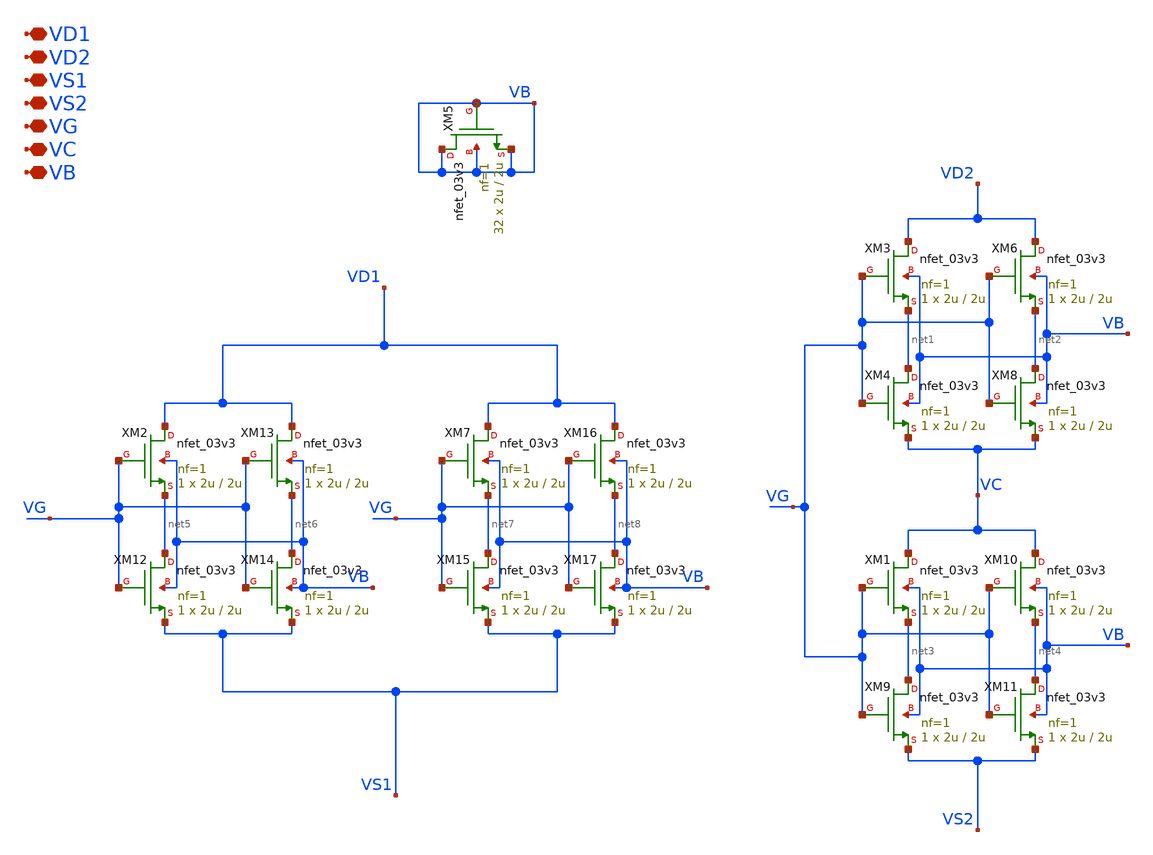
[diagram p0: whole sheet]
** sch_path: TIA_Filter/PseudoResistor/PR_nfets.sch
**.subckt PR_nfets VD1 VD2 VS1 VS2 VG VC VB
*.iopin VD1
*.iopin VD2
*.iopin VS1
*.iopin VS2
*.iopin VG
*.iopin VC
*.iopin VB
XM5 VB VB VB VB nfet_03v3 L=2u W=2u nf=1 ad='int((nf+1)/2) * W/nf * 0.18u' as='int((nf+2)/2) * W/nf * 0.18u'
+ pd='2*int((nf+1)/2) * (W/nf + 0.18u)' ps='2*int((nf+2)/2) * (W/nf + 0.18u)' nrd='0.18u / W' nrs='0.18u / W'
+ sa=0 sb=0 sd=0 m=32
XM3 VD2 VG net1 VB nfet_03v3 L=2u W=2u nf=1 ad='int((nf+1)/2) * W/nf * 0.18u' as='int((nf+2)/2) * W/nf * 0.18u'
+ pd='2*int((nf+1)/2) * (W/nf + 0.18u)' ps='2*int((nf+2)/2) * (W/nf + 0.18u)' nrd='0.18u / W' nrs='0.18u / W'
+ sa=0 sb=0 sd=0 m=1
XM4 net1 VG VC VB nfet_03v3 L=2u W=2u nf=1 ad='int((nf+1)/2) * W/nf * 0.18u' as='int((nf+2)/2) * W/nf * 0.18u'
+ pd='2*int((nf+1)/2) * (W/nf + 0.18u)' ps='2*int((nf+2)/2) * (W/nf + 0.18u)' nrd='0.18u / W' nrs='0.18u / W'
+ sa=0 sb=0 sd=0 m=1
XM6 VD2 VG net2 VB nfet_03v3 L=2u W=2u nf=1 ad='int((nf+1)/2) * W/nf * 0.18u' as='int((nf+2)/2) * W/nf * 0.18u'
+ pd='2*int((nf+1)/2) * (W/nf + 0.18u)' ps='2*int((nf+2)/2) * (W/nf + 0.18u)' nrd='0.18u / W' nrs='0.18u / W'
+ sa=0 sb=0 sd=0 m=1
XM8 net2 VG VC VB nfet_03v3 L=2u W=2u nf=1 ad='int((nf+1)/2) * W/nf * 0.18u' as='int((nf+2)/2) * W/nf * 0.18u'
+ pd='2*int((nf+1)/2) * (W/nf + 0.18u)' ps='2*int((nf+2)/2) * (W/nf + 0.18u)' nrd='0.18u / W' nrs='0.18u / W'
+ sa=0 sb=0 sd=0 m=1
XM1 VC VG net3 VB nfet_03v3 L=2u W=2u nf=1 ad='int((nf+1)/2) * W/nf * 0.18u' as='int((nf+2)/2) * W/nf * 0.18u'
+ pd='2*int((nf+1)/2) * (W/nf + 0.18u)' ps='2*int((nf+2)/2) * (W/nf + 0.18u)' nrd='0.18u / W' nrs='0.18u / W'
+ sa=0 sb=0 sd=0 m=1
XM9 net3 VG VS2 VB nfet_03v3 L=2u W=2u nf=1 ad='int((nf+1)/2) * W/nf * 0.18u' as='int((nf+2)/2) * W/nf * 0.18u'
+ pd='2*int((nf+1)/2) * (W/nf + 0.18u)' ps='2*int((nf+2)/2) * (W/nf + 0.18u)' nrd='0.18u / W' nrs='0.18u / W'
+ sa=0 sb=0 sd=0 m=1
XM10 VC VG net4 VB nfet_03v3 L=2u W=2u nf=1 ad='int((nf+1)/2) * W/nf * 0.18u' as='int((nf+2)/2) * W/nf * 0.18u'
+ pd='2*int((nf+1)/2) * (W/nf + 0.18u)' ps='2*int((nf+2)/2) * (W/nf + 0.18u)' nrd='0.18u / W' nrs='0.18u / W'
+ sa=0 sb=0 sd=0 m=1
XM11 net4 VG VS2 VB nfet_03v3 L=2u W=2u nf=1 ad='int((nf+1)/2) * W/nf * 0.18u' as='int((nf+2)/2) * W/nf * 0.18u'
+ pd='2*int((nf+1)/2) * (W/nf + 0.18u)' ps='2*int((nf+2)/2) * (W/nf + 0.18u)' nrd='0.18u / W' nrs='0.18u / W'
+ sa=0 sb=0 sd=0 m=1
XM2 VD1 VG net5 VB nfet_03v3 L=2u W=2u nf=1 ad='int((nf+1)/2) * W/nf * 0.18u' as='int((nf+2)/2) * W/nf * 0.18u'
+ pd='2*int((nf+1)/2) * (W/nf + 0.18u)' ps='2*int((nf+2)/2) * (W/nf + 0.18u)' nrd='0.18u / W' nrs='0.18u / W'
+ sa=0 sb=0 sd=0 m=1
XM12 net5 VG VS1 VB nfet_03v3 L=2u W=2u nf=1 ad='int((nf+1)/2) * W/nf * 0.18u' as='int((nf+2)/2) * W/nf * 0.18u'
+ pd='2*int((nf+1)/2) * (W/nf + 0.18u)' ps='2*int((nf+2)/2) * (W/nf + 0.18u)' nrd='0.18u / W' nrs='0.18u / W'
+ sa=0 sb=0 sd=0 m=1
XM13 VD1 VG net6 VB nfet_03v3 L=2u W=2u nf=1 ad='int((nf+1)/2) * W/nf * 0.18u' as='int((nf+2)/2) * W/nf * 0.18u'
+ pd='2*int((nf+1)/2) * (W/nf + 0.18u)' ps='2*int((nf+2)/2) * (W/nf + 0.18u)' nrd='0.18u / W' nrs='0.18u / W'
+ sa=0 sb=0 sd=0 m=1
XM14 net6 VG VS1 VB nfet_03v3 L=2u W=2u nf=1 ad='int((nf+1)/2) * W/nf * 0.18u' as='int((nf+2)/2) * W/nf * 0.18u'
+ pd='2*int((nf+1)/2) * (W/nf + 0.18u)' ps='2*int((nf+2)/2) * (W/nf + 0.18u)' nrd='0.18u / W' nrs='0.18u / W'
+ sa=0 sb=0 sd=0 m=1
XM7 VD1 VG net7 VB nfet_03v3 L=2u W=2u nf=1 ad='int((nf+1)/2) * W/nf * 0.18u' as='int((nf+2)/2) * W/nf * 0.18u'
+ pd='2*int((nf+1)/2) * (W/nf + 0.18u)' ps='2*int((nf+2)/2) * (W/nf + 0.18u)' nrd='0.18u / W' nrs='0.18u / W'
+ sa=0 sb=0 sd=0 m=1
XM15 net7 VG VS1 VB nfet_03v3 L=2u W=2u nf=1 ad='int((nf+1)/2) * W/nf * 0.18u' as='int((nf+2)/2) * W/nf * 0.18u'
+ pd='2*int((nf+1)/2) * (W/nf + 0.18u)' ps='2*int((nf+2)/2) * (W/nf + 0.18u)' nrd='0.18u / W' nrs='0.18u / W'
+ sa=0 sb=0 sd=0 m=1
XM16 VD1 VG net8 VB nfet_03v3 L=2u W=2u nf=1 ad='int((nf+1)/2) * W/nf * 0.18u' as='int((nf+2)/2) * W/nf * 0.18u'
+ pd='2*int((nf+1)/2) * (W/nf + 0.18u)' ps='2*int((nf+2)/2) * (W/nf + 0.18u)' nrd='0.18u / W' nrs='0.18u / W'
+ sa=0 sb=0 sd=0 m=1
XM17 net8 VG VS1 VB nfet_03v3 L=2u W=2u nf=1 ad='int((nf+1)/2) * W/nf * 0.18u' as='int((nf+2)/2) * W/nf * 0.18u'
+ pd='2*int((nf+1)/2) * (W/nf + 0.18u)' ps='2*int((nf+2)/2) * (W/nf + 0.18u)' nrd='0.18u / W' nrs='0.18u / W'
+ sa=0 sb=0 sd=0 m=1
**.ends
.end
